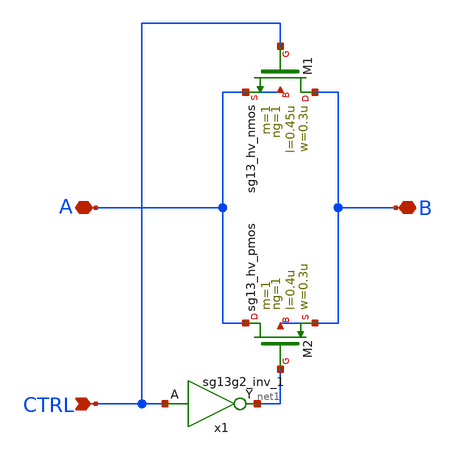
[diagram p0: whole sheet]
** sch_path: ngspice_cosim_tgate/tgate.sch
**.subckt tgate CTRL B A
*.ipin CTRL
*.iopin B
*.iopin A
XM1 B CTRL A A sg13_hv_nmos w=0.3u l=0.45u ng=1 m=1 mm_ok=1
XM2 A net1 B B sg13_hv_pmos w=0.3u l=0.4u ng=1 m=1 mm_ok=1
x1 net1 CTRL VDD VSS sg13g2_inv_1
**.ends

* expanding   symbol:  sg13g2_stdcells/sg13g2_inv_1.sym # of pins=2
** sym_path: sg13g2_stdcells/sg13g2_inv_1.sym
** sch_path: sg13g2_stdcells/sg13g2_inv_1.sch
.subckt sg13g2_inv_1 Y A VDD VSS
*.opin Y
*.ipin A
*.iopin VDD
*.iopin VSS
XM1 Y A VSS VSS sg13_lv_nmos w=740.00n l=130.00n ng=1 m=1 mm_ok=1
XM2 Y A VDD VDD sg13_lv_pmos w=1.12u l=130.00n ng=1 m=1 mm_ok=1
.ends

.end
